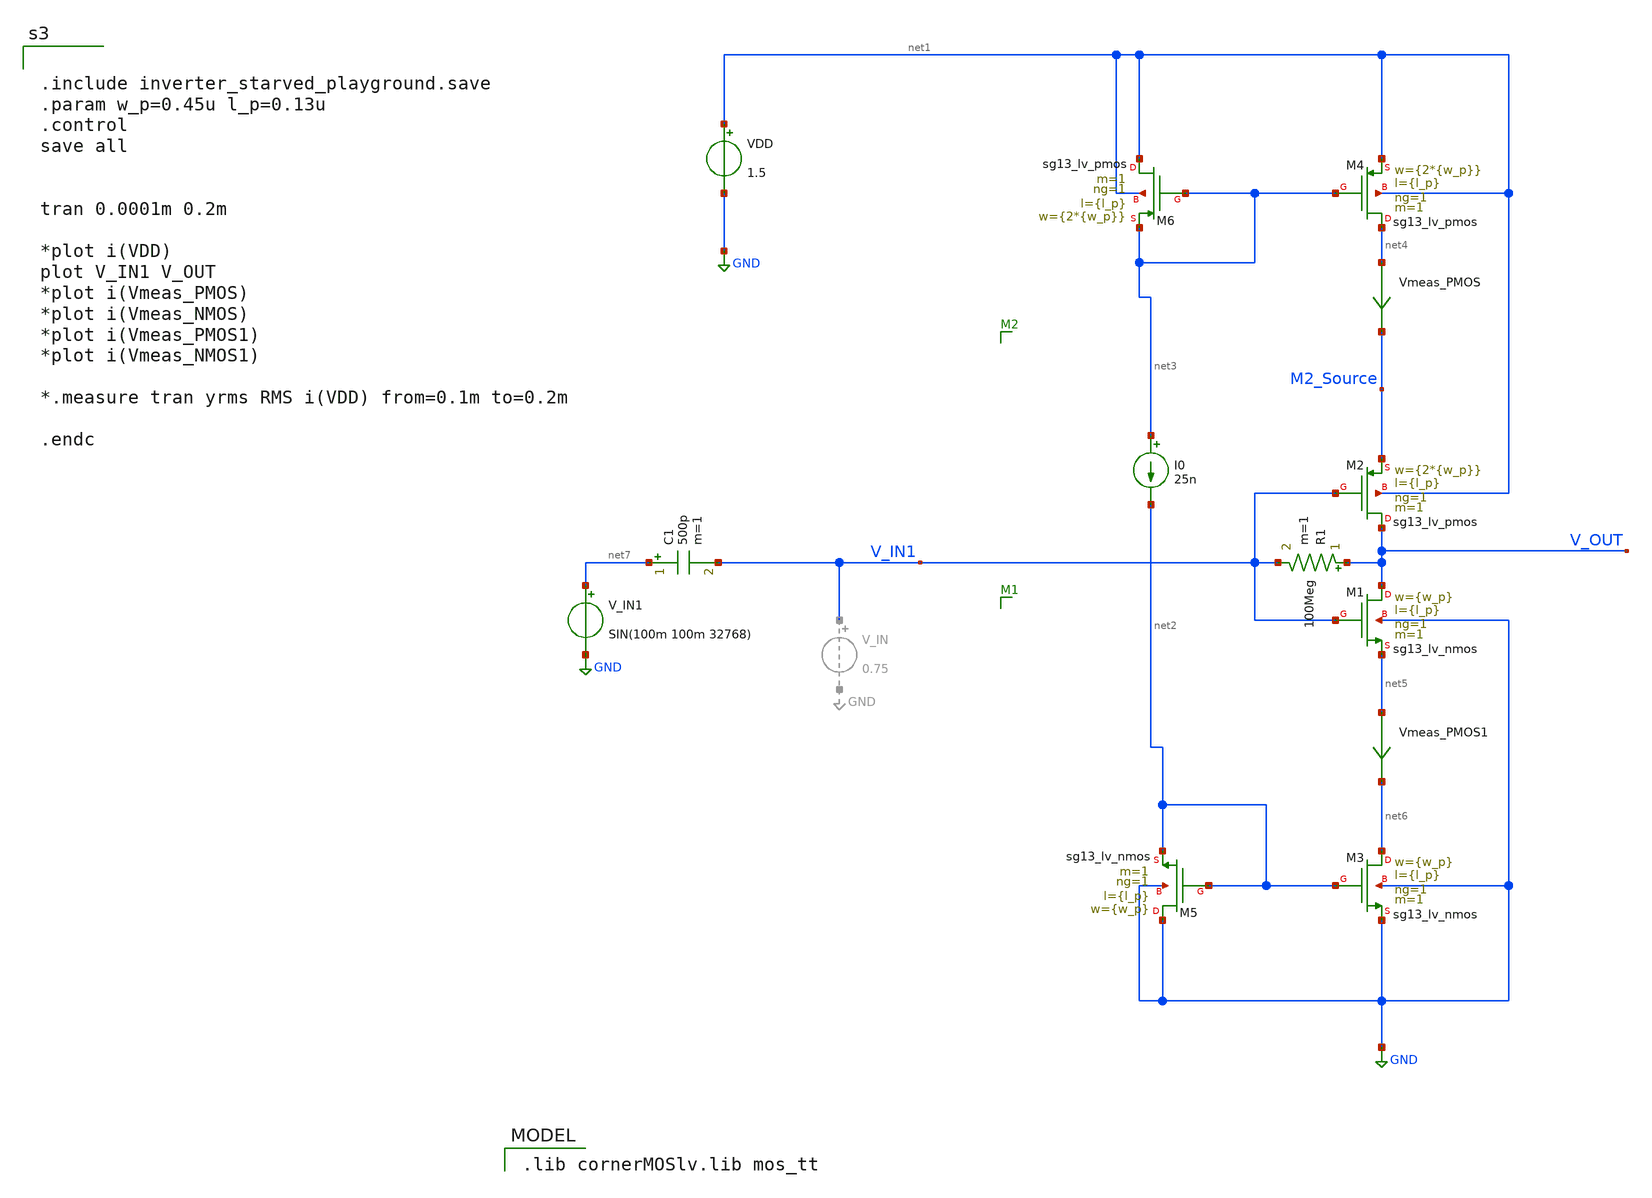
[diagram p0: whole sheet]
** sch_path: inverter_starved_playground.sch
**.subckt inverter_starved_playground
XM1 V_OUT V_IN1 net5 GND sg13_lv_nmos w={w_p} l={l_p} ng=1 m=1 mm_ok=1
XM2 V_OUT V_IN1 M2_Source net1 sg13_lv_pmos w={2*{w_p}} l={l_p} ng=1 m=1 mm_ok=1
VDD net1 GND 1.5
R1 V_OUT V_IN1 100Meg m=1
XM3 net6 net2 GND GND sg13_lv_nmos w={w_p} l={l_p} ng=1 m=1 mm_ok=1
XM4 net4 net3 net1 net1 sg13_lv_pmos w={2*{w_p}} l={l_p} ng=1 m=1 mm_ok=1
XM5 GND net2 net2 GND sg13_lv_nmos w={w_p} l={l_p} ng=1 m=1 mm_ok=1
XM6 net1 net3 net3 net1 sg13_lv_pmos w={2*{w_p}} l={l_p} ng=1 m=1 mm_ok=1
I0 net3 net2 25n
Vmeas_PMOS net4 M2_Source 0
.save i(vmeas_pmos)
Vmeas_PMOS1 net5 net6 0
.save i(vmeas_pmos1)
V_IN1 net7 GND SIN(100m 100m 32768)
C1 net7 V_IN1 500p m=1
**** begin user architecture code
 .lib cornerMOSlv.lib mos_tt



.include inverter_starved_playground.save
.param w_p=0.45u l_p=0.13u
.control
save all


tran 0.0001m 0.2m

*plot i(VDD)
plot V_IN1 V_OUT
*plot i(Vmeas_PMOS)
*plot i(Vmeas_NMOS)
*plot i(Vmeas_PMOS1)
*plot i(Vmeas_NMOS1)

*.measure tran yrms RMS i(VDD) from=0.1m to=0.2m

.endc


**** end user architecture code
**.ends
.GLOBAL GND
.end
